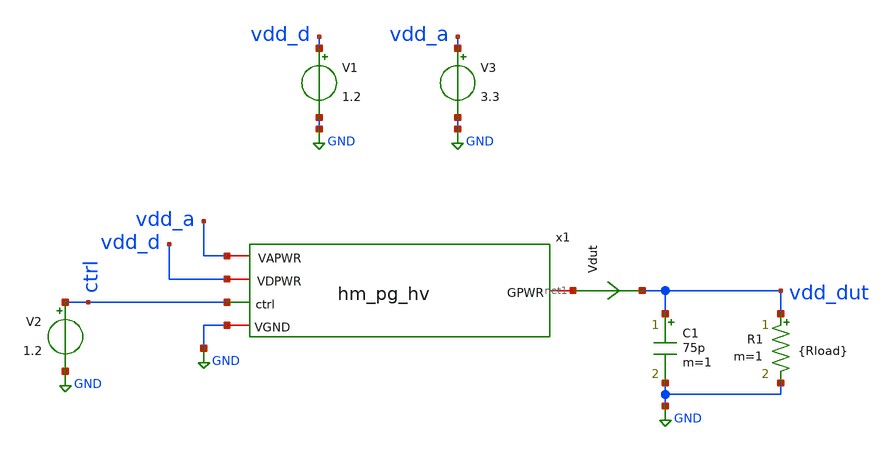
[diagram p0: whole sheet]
** sch_path: ihp-sg13cmos5l/libs.tech/xschem/tests/tb_hm_pg_hv.sch
**.subckt tb_hm_pg_hv
V1 vdd_d GND 1.2
.save i(v1)
V2 ctrl GND 1.2
C1 vdd_dut GND 75p m=1
Vdut net1 vdd_dut 0
.save i(vdut)
R1 vdd_dut GND {Rload} m=1
x1 net1 vdd_a vdd_d ctrl GND hm_pg_hv
V3 vdd_a GND 3.3
.save i(v3)
**** begin user architecture code

.lib cornerMOShv.lib mos_tt
.lib cornerMOSlv.lib mos_tt
*.lib cornerCAP.lib cap_typ



.param Rload=1000

.control

let npoints = 8
let rvec = vector(npoints)
let ivec = vector(npoints)
let vdrop_vec = vector(npoints)
let ron_vec = vector(npoints)

let vdd_dutvec = vector(npoints)

let idx=0

foreach r 10000 5000 2000 1000 500 200 100 10
  alterparam Rload=$r
  reset
  save all
  op

  let iload = i(vdut)
  let vdrop = v(vdd_a) - v(vdd_dut)
  let ron = vdrop/iload

  let rvec[idx] = $r
  let ivec[idx] = iload
  let vdrop_vec[idx] = vdrop
  let ron_vec[idx] = ron

  let vdd_dutvec[idx] = vdd_dut

  echo -------------------------
  echo Rload = $r
  print iload vdrop ron
  print x1.H_crtl_p

  let idx = idx + 1
end

plot ron_vec vs ivec
plot vdd_dutvec vs ivec
plot vdd_dut

.endc


**** end user architecture code
**.ends

* expanding   symbol:
*+  /foss/designs/hm-openpdk-library/ihp-sg13cmos5l/libs.tech/xschem/hm_analog/hm_pg_hv.sym # of pins=5
** sym_path: ihp-sg13cmos5l/libs.tech/xschem/hm_analog/hm_pg_hv.sym
** sch_path: ihp-sg13cmos5l/libs.tech/xschem/hm_analog/hm_pg_hv.sch
.subckt hm_pg_hv GPWR VAPWR VDPWR ctrl VGND
*.ipin ctrl
*.iopin VAPWR
*.iopin VGND
*.iopin GPWR
*.iopin VDPWR
x2 VAPWR VDPWR ctrl H_crtl_p H_crtl_n VGND lv2hv
XM4 ctrl_n H_crtl_p VGND VGND sg13_hv_nmos w=2.6u l=0.45u ng=1 m=1 mm_ok=1
XM5 ctrl_n H_crtl_p VAPWR VAPWR sg13_hv_pmos w=4.44u l=0.45u ng=1 m=1 mm_ok=1
XM1 GPWR ctrl_n VAPWR VAPWR sg13_hv_pmos w=1445.4u l=0.45u ng=219 m=2 mm_ok=1
x3 VGND GPWR ctrl_n hv_dischg
.ends


* expanding   symbol:
*+  /foss/designs/hm-openpdk-library/ihp-sg13cmos5l/libs.tech/xschem/hm_analog/lv2hv.sym # of pins=6
** sym_path: ihp-sg13cmos5l/libs.tech/xschem/hm_analog/lv2hv.sym
** sch_path: ihp-sg13cmos5l/libs.tech/xschem/hm_analog/lv2hv.sch
.subckt lv2hv VAPWR VDPWR in out_p out_n VGND
*.iopin VAPWR
*.iopin VGND
*.ipin in
*.iopin VDPWR
*.opin out_p
*.opin out_n
XM1 in_n in VGND VGND sg13_lv_nmos w=1u l=0.13u ng=1 m=1 mm_ok=1
XM2 in_n in VDPWR VDPWR sg13_lv_pmos w=2u l=0.13u ng=1 m=1 mm_ok=1
XM3 in_p in_n VGND VGND sg13_lv_nmos w=1u l=0.13u ng=1 m=1 mm_ok=1
XM4 in_p in_n VDPWR VDPWR sg13_lv_pmos w=2u l=0.13u ng=1 m=1 mm_ok=1
XM5 out_p ccp VGND VGND sg13_hv_nmos w=1u l=0.45u ng=1 m=1 mm_ok=1
XM6 ccp in_p VGND VGND sg13_hv_nmos w=4u l=0.45u ng=1 m=1 mm_ok=1
XM7 out_p ccp VAPWR VAPWR sg13_hv_pmos w=2u l=0.45u ng=1 m=1 mm_ok=1
XM8 ccp ccn VAPWR VAPWR sg13_hv_pmos w=1u l=0.4u ng=1 m=1 mm_ok=1
XM9 ccn ccp VAPWR VAPWR sg13_hv_pmos w=1u l=0.4u ng=1 m=1 mm_ok=1
XM10 ccn in_n VGND VGND sg13_hv_nmos w=4u l=0.45u ng=1 m=1 mm_ok=1
XM11 out_n ccn VGND VGND sg13_hv_nmos w=1u l=0.45u ng=1 m=1 mm_ok=1
XM12 out_n ccn VAPWR VAPWR sg13_hv_pmos w=2u l=0.45u ng=1 m=1 mm_ok=1
.ends


* expanding   symbol:
*+  /foss/designs/hm-openpdk-library/ihp-sg13cmos5l/libs.tech/xschem/hm_analog/hv_dischg.sym # of pins=3
** sym_path: ihp-sg13cmos5l/libs.tech/xschem/hm_analog/hv_dischg.sym
** sch_path: ihp-sg13cmos5l/libs.tech/xschem/hm_analog/hv_dischg.sch
.subckt hv_dischg VGND GPWR gate
*.iopin GPWR
*.iopin VGND
*.ipin gate
XM6 GPWR gate net6 VGND sg13_hv_nmos w=0.5u l=0.65u ng=1 m=1 mm_ok=1
XM7 net6 gate net5 VGND sg13_hv_nmos w=0.5u l=0.65u ng=1 m=1 mm_ok=1
XM8 net5 gate net4 VGND sg13_hv_nmos w=0.5u l=0.65u ng=1 m=1 mm_ok=1
XM9 net4 gate VGND VGND sg13_hv_nmos w=0.5u l=0.65u ng=1 m=1 mm_ok=1
XM1 GPWR gate net1 VGND sg13_hv_nmos w=0.5u l=0.65u ng=1 m=1 mm_ok=1
XM2 net1 gate net2 VGND sg13_hv_nmos w=0.5u l=0.65u ng=1 m=1 mm_ok=1
XM3 net2 gate net3 VGND sg13_hv_nmos w=0.5u l=0.65u ng=1 m=1 mm_ok=1
XM4 net3 gate VGND VGND sg13_hv_nmos w=0.5u l=0.65u ng=1 m=1 mm_ok=1
.ends

.GLOBAL GND
.end
